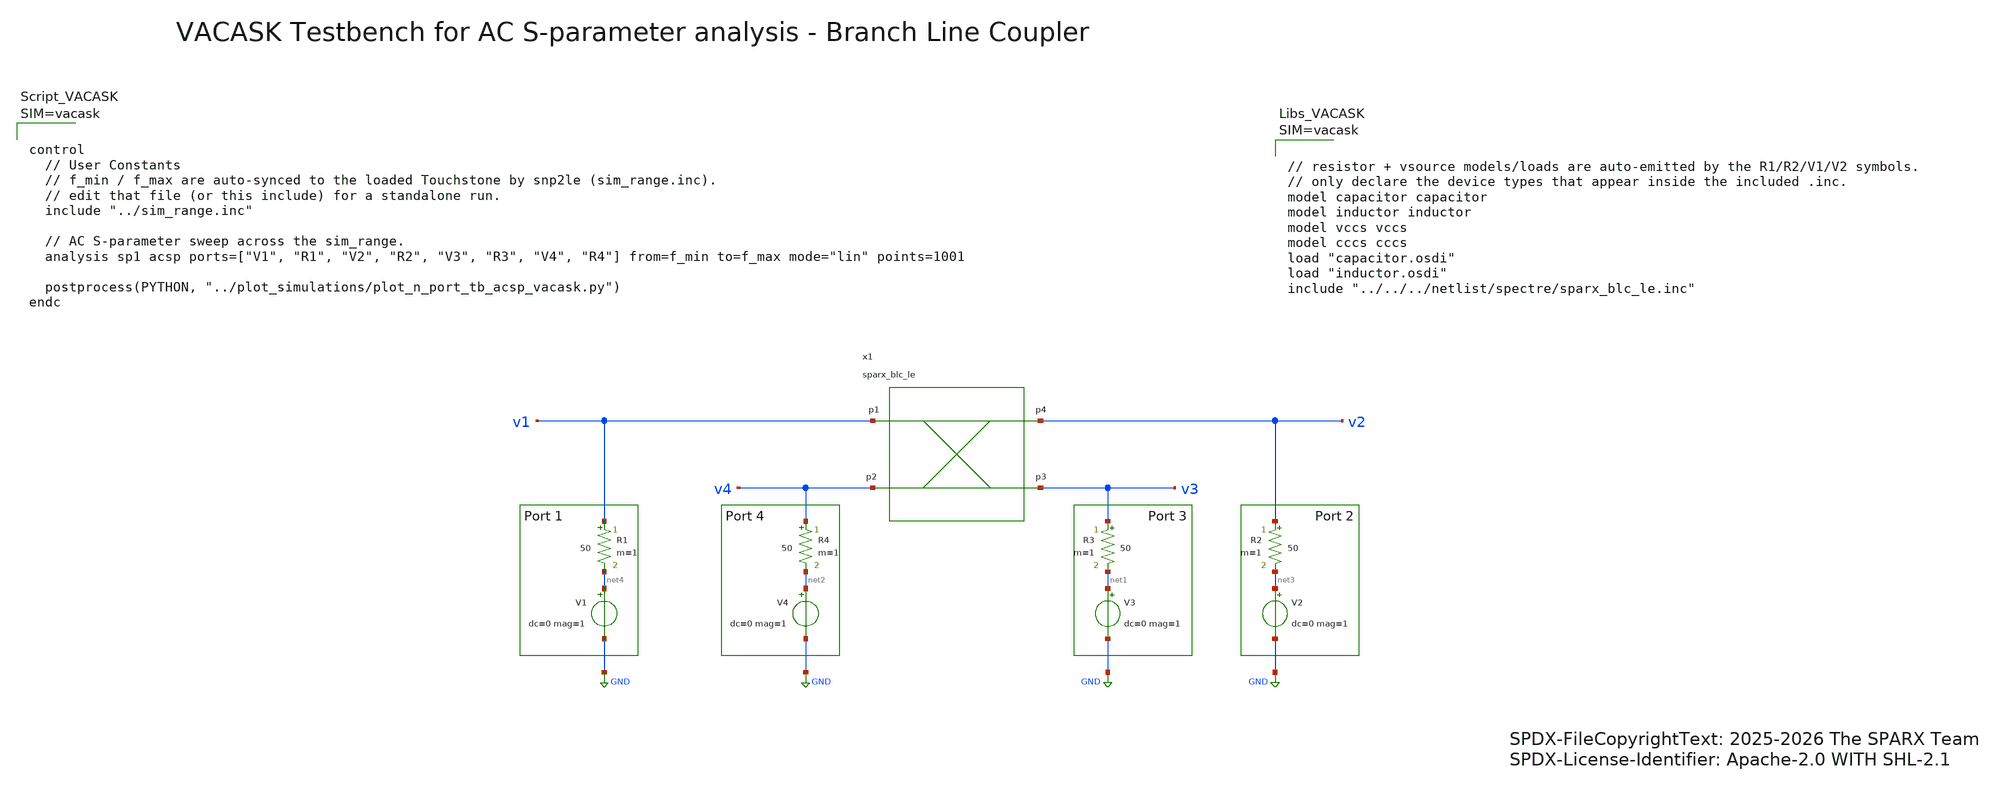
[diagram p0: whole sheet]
** sch_path: testbenches/xschem/sparx_blc_le_tb_acsp_vacask.sch
* SPDX-FileCopyrightText: 2025-2026 The SPARX Team
* SPDX-License-Identifier: Apache-2.0 WITH SHL-2.1
**.subckt sparx_blc_le_tb_acsp_vacask
R3 v3 net1 50 m=1
V3 net1 GND dc=0 mag=1
R4 v4 net2 50 m=1
V4 net2 GND dc=0 mag=1
R1 v1 net4 50 m=1
V1 net4 GND dc=0 mag=1
R2 v2 net3 50 m=1
V2 net3 GND dc=0 mag=1
x1 v1 v4 v3 v2 sparx_blc_le
**** begin user architecture code






**** end user architecture code
**.ends
.GLOBAL GND
.end
